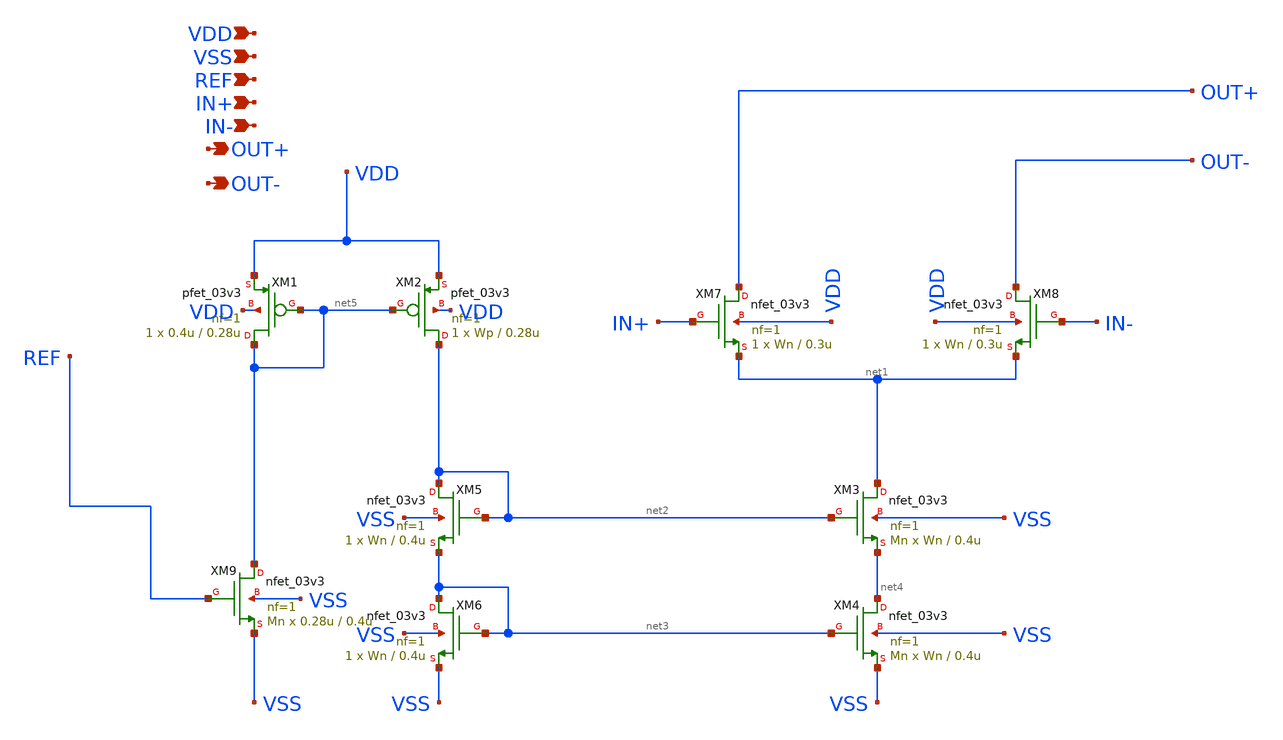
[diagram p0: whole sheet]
** sch_path: DAC/xschem/analog_cell/current_unit.sch
**.subckt current_unit REF IN+ IN- OUT+ OUT- VSS VDD
*.ipin REF
*.ipin IN+
*.ipin IN-
*.opin OUT+
*.opin OUT-
*.ipin VSS
*.ipin VDD
XM3 net1 net2 net4 VSS nfet_03v3 L=0.4u W=Wn nf=1 ad='int((nf+1)/2) * W/nf * 0.18u' as='int((nf+2)/2) * W/nf * 0.18u'
+ pd='2*int((nf+1)/2) * (W/nf + 0.18u)' ps='2*int((nf+2)/2) * (W/nf + 0.18u)' nrd='0.18u / W' nrs='0.18u / W'
+ sa=0 sb=0 sd=0 m=Mn
XM4 net4 net3 VSS VSS nfet_03v3 L=0.4u W=Wn nf=1 ad='int((nf+1)/2) * W/nf * 0.18u' as='int((nf+2)/2) * W/nf * 0.18u'
+ pd='2*int((nf+1)/2) * (W/nf + 0.18u)' ps='2*int((nf+2)/2) * (W/nf + 0.18u)' nrd='0.18u / W' nrs='0.18u / W'
+ sa=0 sb=0 sd=0 m=Mn
XM5 net2 net2 net3 VSS nfet_03v3 L=0.4u W=Wn nf=1 ad='int((nf+1)/2) * W/nf * 0.18u' as='int((nf+2)/2) * W/nf * 0.18u'
+ pd='2*int((nf+1)/2) * (W/nf + 0.18u)' ps='2*int((nf+2)/2) * (W/nf + 0.18u)' nrd='0.18u / W' nrs='0.18u / W'
+ sa=0 sb=0 sd=0 m=1
XM6 net3 net3 VSS VSS nfet_03v3 L=0.4u W=Wn nf=1 ad='int((nf+1)/2) * W/nf * 0.18u' as='int((nf+2)/2) * W/nf * 0.18u'
+ pd='2*int((nf+1)/2) * (W/nf + 0.18u)' ps='2*int((nf+2)/2) * (W/nf + 0.18u)' nrd='0.18u / W' nrs='0.18u / W'
+ sa=0 sb=0 sd=0 m=1
XM1 net5 net5 VDD VDD pfet_03v3 L=0.28u W=0.4u nf=1 ad='int((nf+1)/2) * W/nf * 0.18u' as='int((nf+2)/2) * W/nf * 0.18u'
+ pd='2*int((nf+1)/2) * (W/nf + 0.18u)' ps='2*int((nf+2)/2) * (W/nf + 0.18u)' nrd='0.18u / W' nrs='0.18u / W'
+ sa=0 sb=0 sd=0 m=1
XM2 net2 net5 VDD VDD pfet_03v3 L=0.28u W=Wp nf=1 ad='int((nf+1)/2) * W/nf * 0.18u' as='int((nf+2)/2) * W/nf * 0.18u'
+ pd='2*int((nf+1)/2) * (W/nf + 0.18u)' ps='2*int((nf+2)/2) * (W/nf + 0.18u)' nrd='0.18u / W' nrs='0.18u / W'
+ sa=0 sb=0 sd=0 m=1
XM7 OUT+ IN+ net1 VDD nfet_03v3 L=0.3u W=Wn nf=1 ad='int((nf+1)/2) * W/nf * 0.18u' as='int((nf+2)/2) * W/nf * 0.18u'
+ pd='2*int((nf+1)/2) * (W/nf + 0.18u)' ps='2*int((nf+2)/2) * (W/nf + 0.18u)' nrd='0.18u / W' nrs='0.18u / W'
+ sa=0 sb=0 sd=0 m=1
XM8 OUT- IN- net1 VDD nfet_03v3 L=0.3u W=Wn nf=1 ad='int((nf+1)/2) * W/nf * 0.18u' as='int((nf+2)/2) * W/nf * 0.18u'
+ pd='2*int((nf+1)/2) * (W/nf + 0.18u)' ps='2*int((nf+2)/2) * (W/nf + 0.18u)' nrd='0.18u / W' nrs='0.18u / W'
+ sa=0 sb=0 sd=0 m=1
XM9 net5 REF VSS VSS nfet_03v3 L=0.4u W=0.28u nf=1 ad='int((nf+1)/2) * W/nf * 0.18u' as='int((nf+2)/2) * W/nf * 0.18u'
+ pd='2*int((nf+1)/2) * (W/nf + 0.18u)' ps='2*int((nf+2)/2) * (W/nf + 0.18u)' nrd='0.18u / W' nrs='0.18u / W'
+ sa=0 sb=0 sd=0 m=Mn
**.ends
.end
